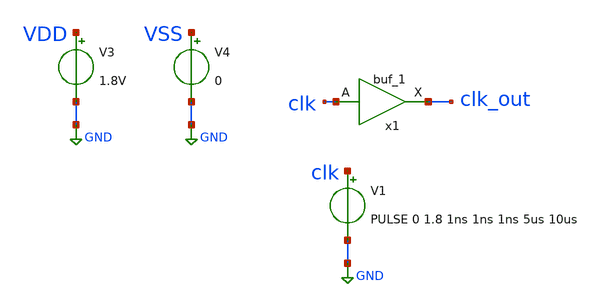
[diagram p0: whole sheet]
** sch_path: xschem/tests/dummy_tests/dummy2.sch
**.subckt dummy2
V3 VDD GND 1.8V
V4 VSS GND 0
V1 clk GND PULSE 0 1.8 1ns 1ns 1ns 5us 10us
x1 clk VSS VSS VDD VDD clk_out sky130_fd_sc_hd__buf_1
**** begin user architecture code
 .lib $::SKYWATER_MODELS/sky130.lib.spice tt
.include $::SKYWATER_STDCELLS/sky130_fd_sc_hd.spice


.options acct list
.temp 25
*vvcc VDD 0 dc 1.8
*vvss VSS 0 0
.control
tran 0.1p 4n
*plot RST_PLS clk+2 Pulse+4
plot clk clk_out
write dummy2.raw
.endc


**** end user architecture code
**.ends
.GLOBAL GND
.end
